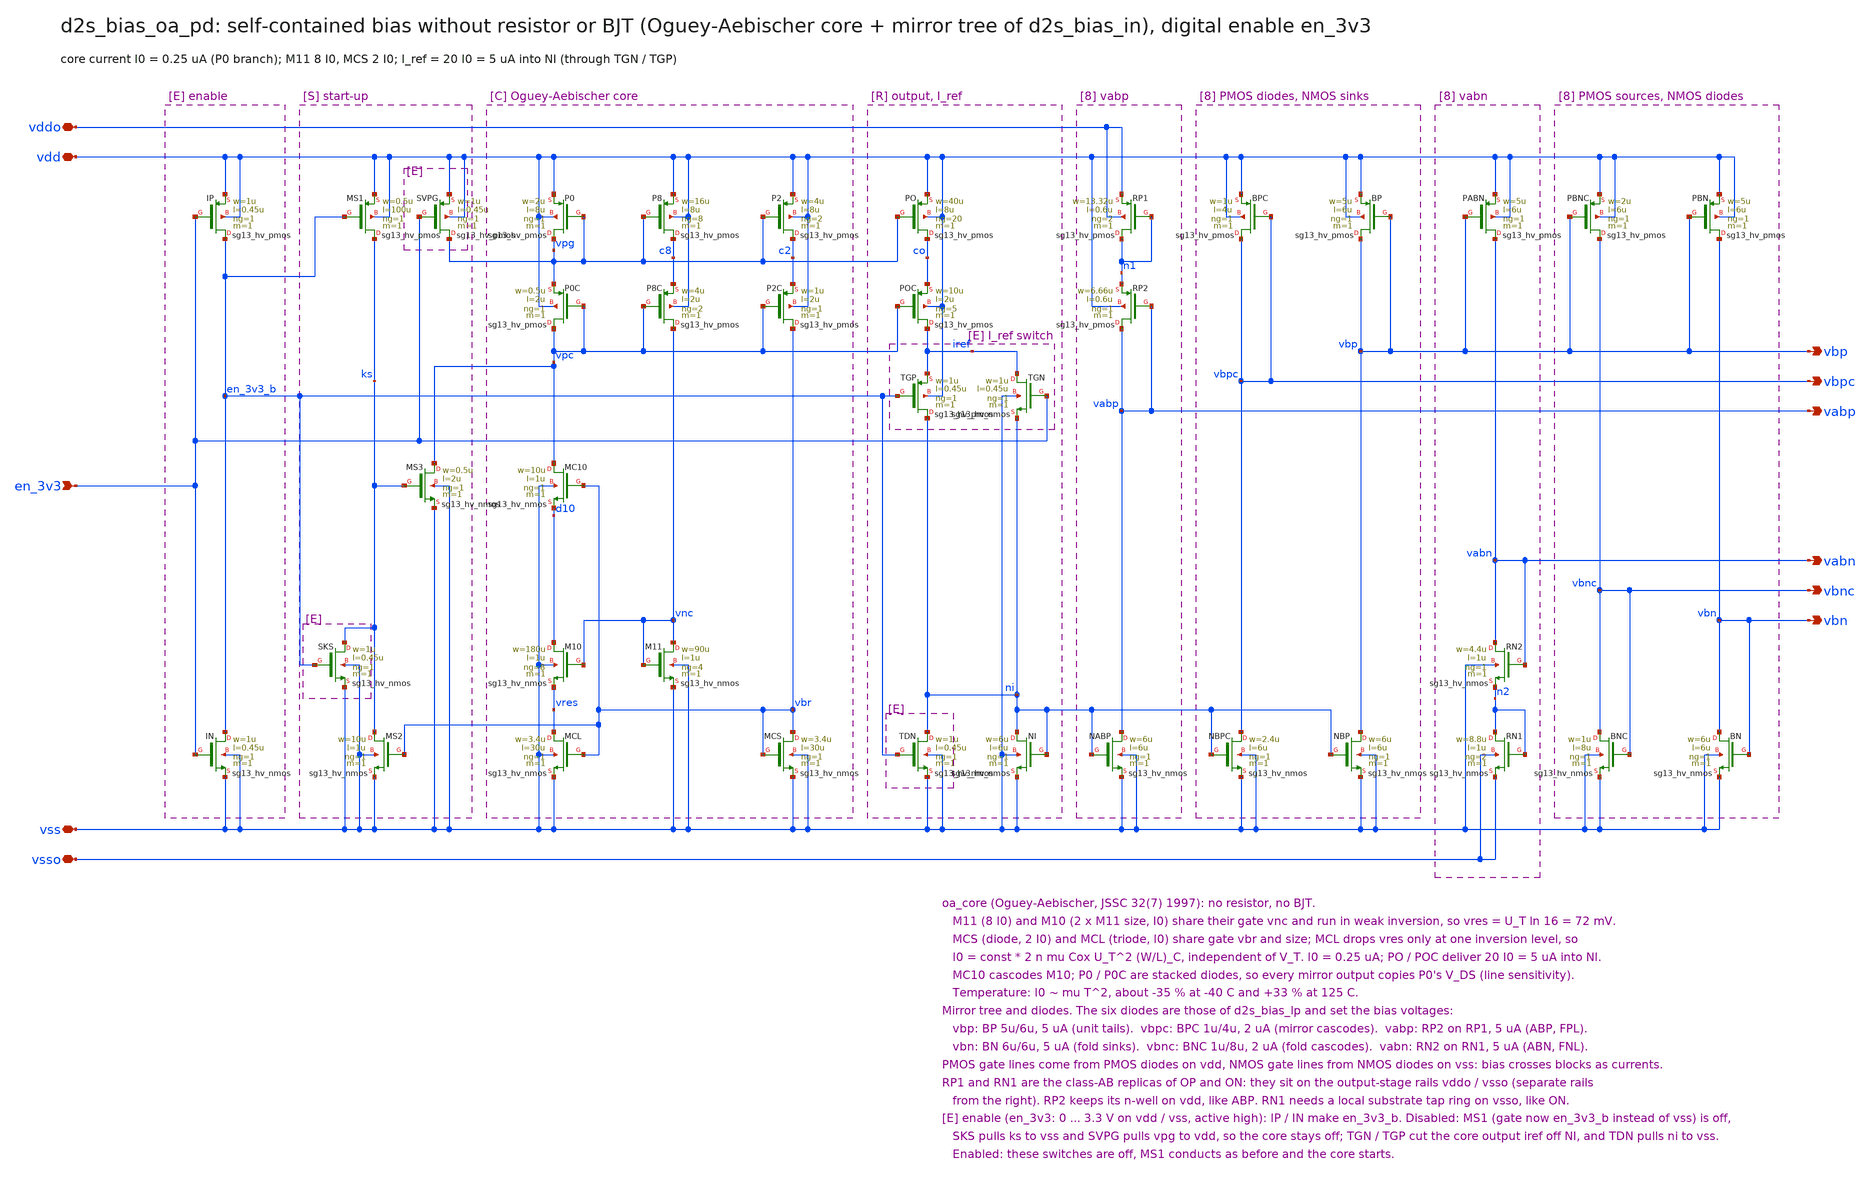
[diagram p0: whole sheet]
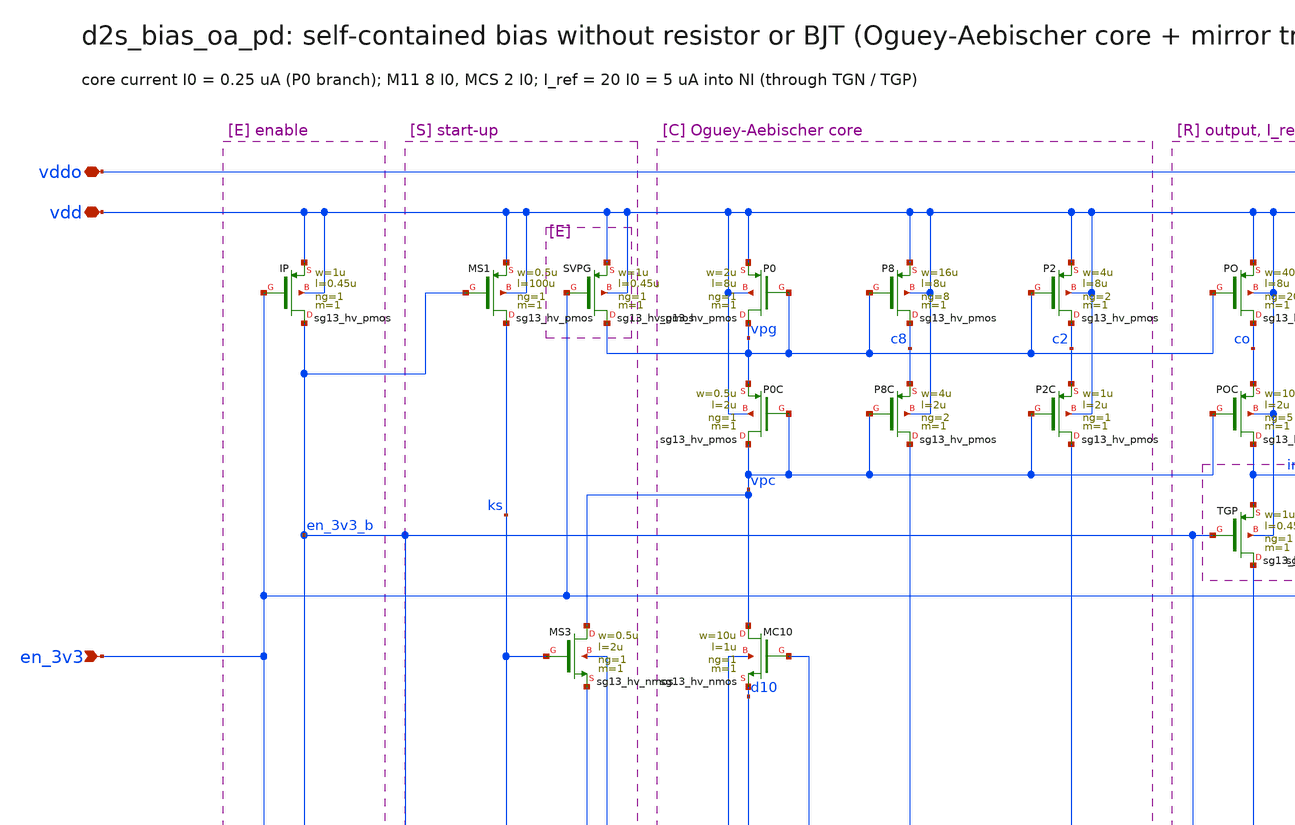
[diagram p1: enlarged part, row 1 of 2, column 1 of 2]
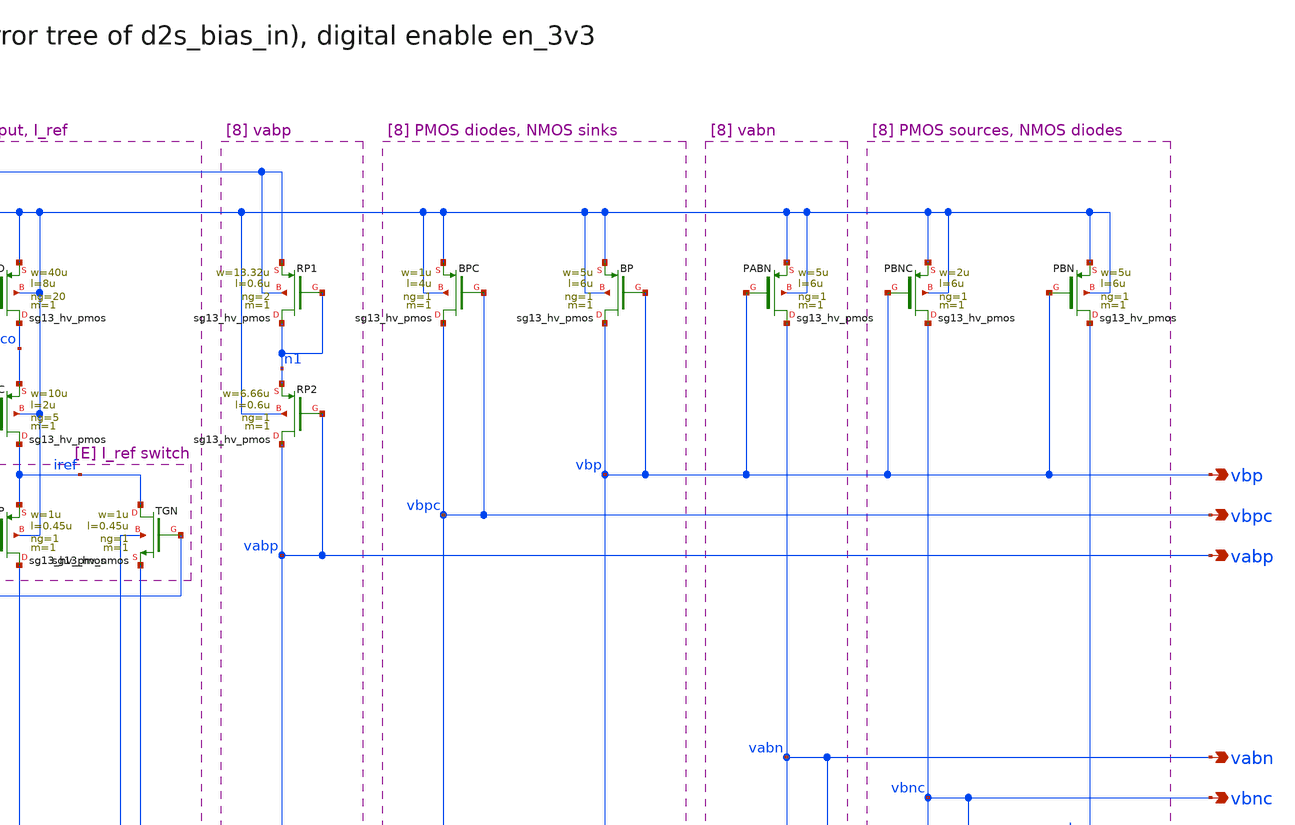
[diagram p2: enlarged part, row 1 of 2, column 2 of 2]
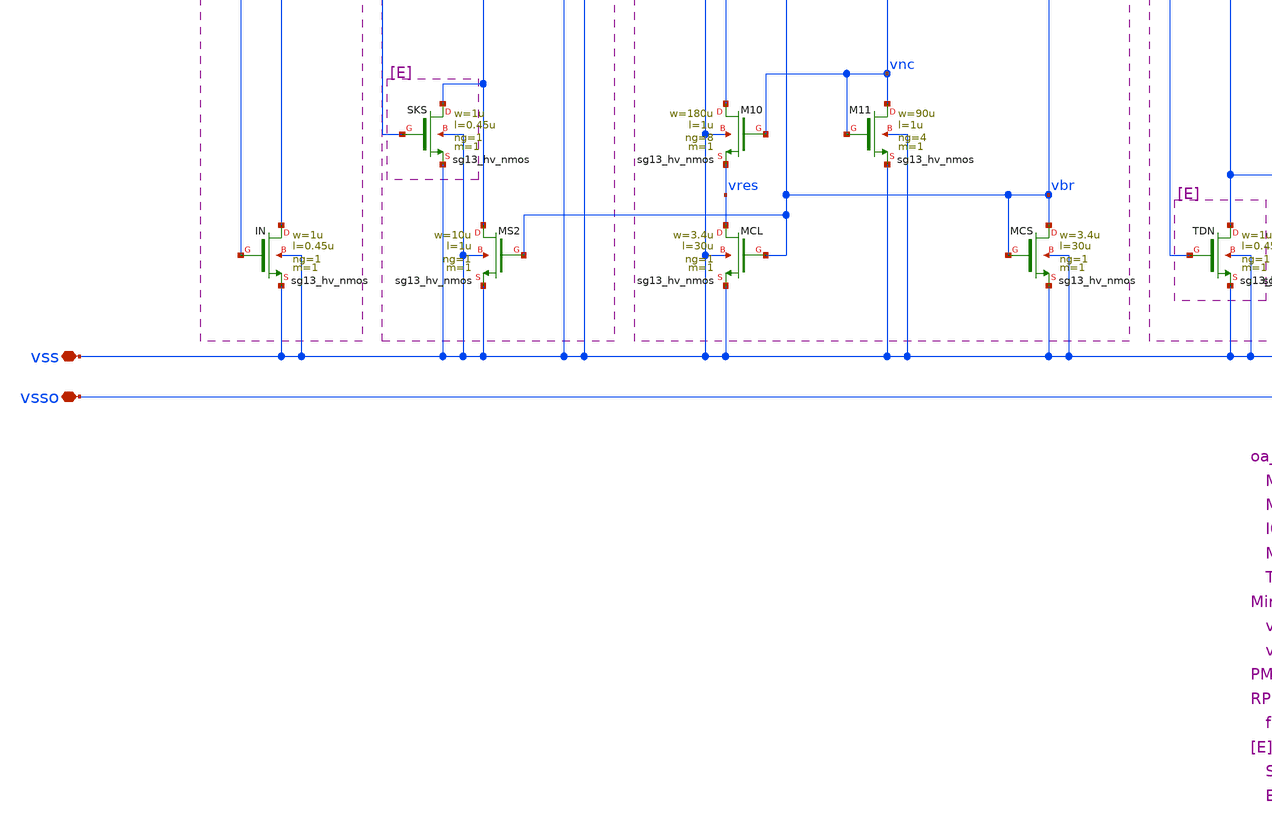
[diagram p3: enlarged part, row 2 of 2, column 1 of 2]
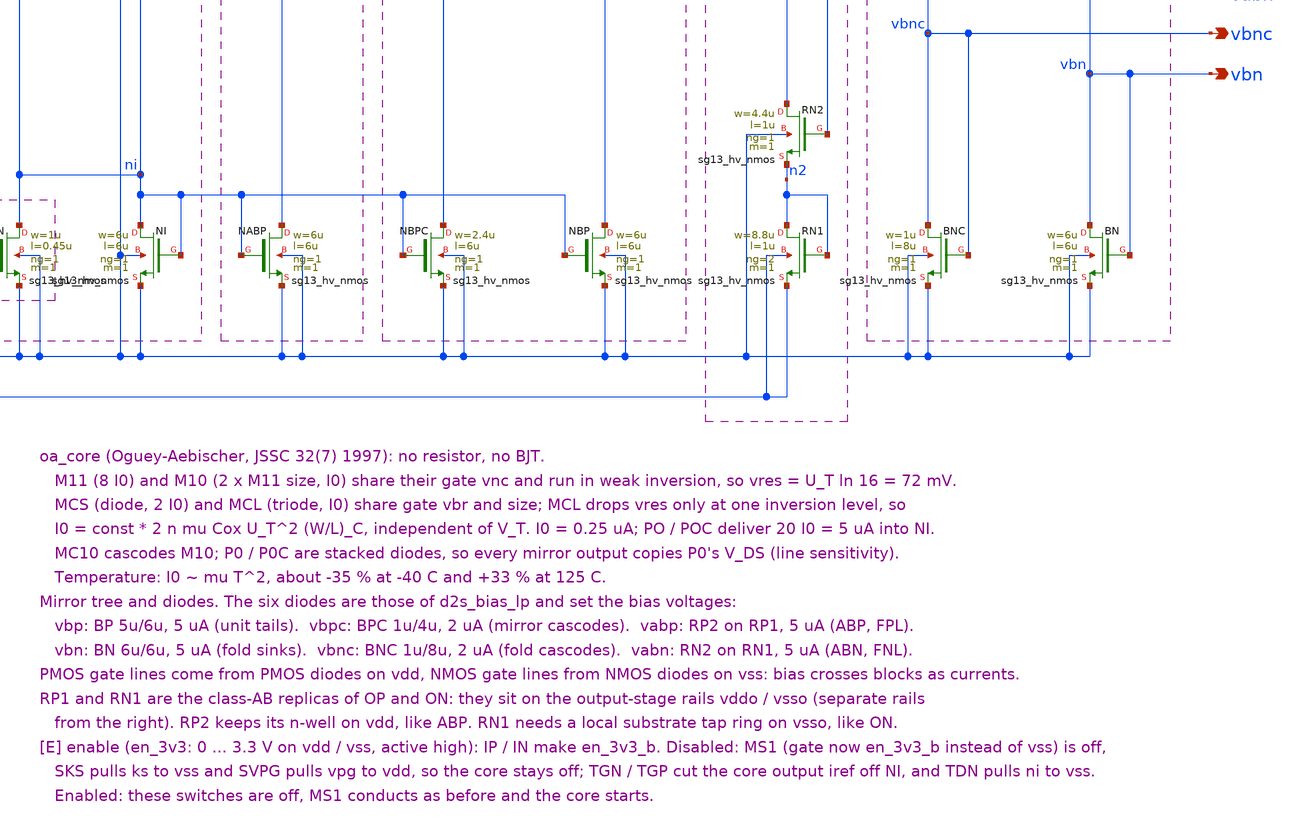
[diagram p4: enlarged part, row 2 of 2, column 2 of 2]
** sch_path: sudelbuecher/design_considerations/consolidation/bias_hierarchy_2026-10-27/before/macros/d2s_bias_oa_pd/schematic/xschem/d2s_bias_oa_pd.sch
**.subckt d2s_bias_oa_pd vdd vss vddo vsso vbp vbn vbpc vbnc vabp vabn en_3v3
*.iopin vdd
*.iopin vss
*.iopin vddo
*.iopin vsso
*.opin vbp
*.opin vbn
*.opin vbpc
*.opin vbnc
*.opin vabp
*.opin vabn
*.ipin en_3v3
XMS1 ks en_3v3_b vdd vdd sg13_hv_pmos w=0.5u l=100u ng=1 m=1 mm_ok=1
XMS2 ks vbr vss vss sg13_hv_nmos w=10u l=1u ng=1 m=1 mm_ok=1
XMS3 vpc ks vss vss sg13_hv_nmos w=0.5u l=2u ng=1 m=1 mm_ok=1
XP0 vpg vpg vdd vdd sg13_hv_pmos w=2u l=8u ng=1 m=1 mm_ok=1
XP0C vpc vpc vpg vdd sg13_hv_pmos w=0.5u l=2u ng=1 m=1 mm_ok=1
XMC10 vpc vbr d10 vss sg13_hv_nmos w=10u l=1u ng=1 m=1 mm_ok=1
XM10 d10 vnc vres vss sg13_hv_nmos w=180u l=1u ng=8 m=1 mm_ok=1
XMCL vres vbr vss vss sg13_hv_nmos w=3.4u l=30u ng=1 m=1 mm_ok=1
XP8 c8 vpg vdd vdd sg13_hv_pmos w=16u l=8u ng=8 m=1 mm_ok=1
XP8C vnc vpc c8 vdd sg13_hv_pmos w=4u l=2u ng=2 m=1 mm_ok=1
XM11 vnc vnc vss vss sg13_hv_nmos w=90u l=1u ng=4 m=1 mm_ok=1
XP2 c2 vpg vdd vdd sg13_hv_pmos w=4u l=8u ng=2 m=1 mm_ok=1
XP2C vbr vpc c2 vdd sg13_hv_pmos w=1u l=2u ng=1 m=1 mm_ok=1
XMCS vbr vbr vss vss sg13_hv_nmos w=3.4u l=30u ng=1 m=1 mm_ok=1
XPO co vpg vdd vdd sg13_hv_pmos w=40u l=8u ng=20 m=1 mm_ok=1
XPOC iref vpc co vdd sg13_hv_pmos w=10u l=2u ng=5 m=1 mm_ok=1
XNI ni ni vss vss sg13_hv_nmos w=6u l=6u ng=1 m=1 mm_ok=1
XBPC vbpc vbpc vdd vdd sg13_hv_pmos w=1u l=4u ng=1 m=1 mm_ok=1
XNBPC vbpc ni vss vss sg13_hv_nmos w=2.4u l=6u ng=1 m=1 mm_ok=1
XBP vbp vbp vdd vdd sg13_hv_pmos w=5u l=6u ng=1 m=1 mm_ok=1
XNBP vbp ni vss vss sg13_hv_nmos w=6u l=6u ng=1 m=1 mm_ok=1
XRP1 n1 n1 vddo vddo sg13_hv_pmos w=13.32u l=0.6u ng=2 m=1 mm_ok=1
XRP2 vabp vabp n1 vdd sg13_hv_pmos w=6.66u l=0.6u ng=1 m=1 mm_ok=1
XNABP vabp ni vss vss sg13_hv_nmos w=6u l=6u ng=1 m=1 mm_ok=1
XPBNC vbnc vbp vdd vdd sg13_hv_pmos w=2u l=6u ng=1 m=1 mm_ok=1
XBNC vbnc vbnc vss vss sg13_hv_nmos w=1u l=8u ng=1 m=1 mm_ok=1
XPBN vbn vbp vdd vdd sg13_hv_pmos w=5u l=6u ng=1 m=1 mm_ok=1
XBN vbn vbn vss vss sg13_hv_nmos w=6u l=6u ng=1 m=1 mm_ok=1
XPABN vabn vbp vdd vdd sg13_hv_pmos w=5u l=6u ng=1 m=1 mm_ok=1
XRN2 vabn vabn n2 vss sg13_hv_nmos w=4.4u l=1u ng=1 m=1 mm_ok=1
XRN1 n2 n2 vsso vsso sg13_hv_nmos w=8.8u l=1u ng=2 m=1 mm_ok=1
XSKS ks en_3v3_b vss vss sg13_hv_nmos w=1u l=0.45u ng=1 m=1 mm_ok=1
XSVPG vpg en_3v3 vdd vdd sg13_hv_pmos w=1u l=0.45u ng=1 m=1 mm_ok=1
XTDN ni en_3v3_b vss vss sg13_hv_nmos w=1u l=0.45u ng=1 m=1 mm_ok=1
XIP en_3v3_b en_3v3 vdd vdd sg13_hv_pmos w=1u l=0.45u ng=1 m=1 mm_ok=1
XIN en_3v3_b en_3v3 vss vss sg13_hv_nmos w=1u l=0.45u ng=1 m=1 mm_ok=1
XTGP ni en_3v3_b iref vdd sg13_hv_pmos w=1u l=0.45u ng=1 m=1 mm_ok=1
XTGN iref en_3v3 ni vss sg13_hv_nmos w=1u l=0.45u ng=1 m=1 mm_ok=1
**.ends
.end
